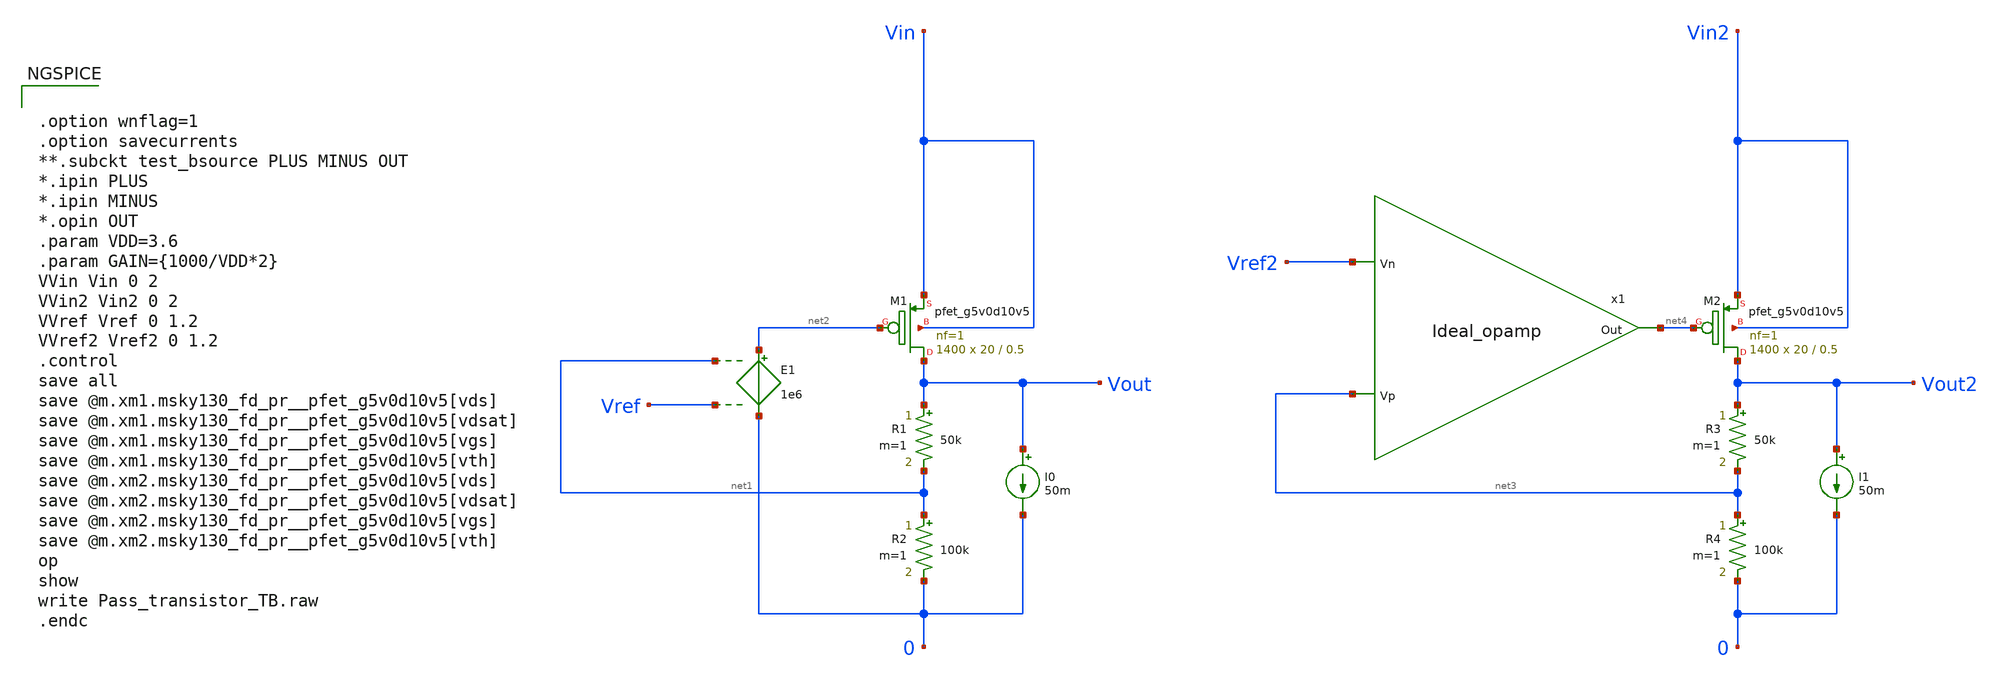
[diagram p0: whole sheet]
** sch_path: Analog_Blocks/LDO/Testbench/Pass_transistor_TB.sch
**.subckt Pass_transistor_TB
XM1 Vout net2 Vin Vin sky130_fd_pr__pfet_g5v0d10v5 L=0.5 W=20 nf=1 ad='int((nf+1)/2) * W/nf * 0.29' as='int((nf+2)/2) * W/nf * 0.29'
+ pd='2*int((nf+1)/2) * (W/nf + 0.29)' ps='2*int((nf+2)/2) * (W/nf + 0.29)' nrd='0.29 / W' nrs='0.29 / W'
+ sa=0 sb=0 sd=0 mult=1400 m=1400
R1 Vout net1 50k m=1
R2 net1 0 100k m=1
E1 net2 0 net1 Vref 1e6
I0 Vout 0 50m
XM2 Vout2 net4 Vin2 Vin2 sky130_fd_pr__pfet_g5v0d10v5 L=0.5 W=20 nf=1 ad='int((nf+1)/2) * W/nf * 0.29'
+ as='int((nf+2)/2) * W/nf * 0.29' pd='2*int((nf+1)/2) * (W/nf + 0.29)' ps='2*int((nf+2)/2) * (W/nf + 0.29)'
+ nrd='0.29 / W' nrs='0.29 / W' sa=0 sb=0 sd=0 mult=1400 m=1400
R3 Vout2 net3 50k m=1
R4 net3 0 100k m=1
I1 Vout2 0 50m
x1 net3 net4 Vref2 Ideal_opamp
**** begin user architecture code


.option wnflag=1
.option savecurrents
**.subckt test_bsource PLUS MINUS OUT
*.ipin PLUS
*.ipin MINUS
*.opin OUT
.param VDD=3.6
.param GAIN={1000/VDD*2}
VVin Vin 0 2
VVin2 Vin2 0 2
VVref Vref 0 1.2
VVref2 Vref2 0 1.2
.control
save all
save @m.xm1.msky130_fd_pr__pfet_g5v0d10v5[vds]
save @m.xm1.msky130_fd_pr__pfet_g5v0d10v5[vdsat]
save @m.xm1.msky130_fd_pr__pfet_g5v0d10v5[vgs]
save @m.xm1.msky130_fd_pr__pfet_g5v0d10v5[vth]
save @m.xm2.msky130_fd_pr__pfet_g5v0d10v5[vds]
save @m.xm2.msky130_fd_pr__pfet_g5v0d10v5[vdsat]
save @m.xm2.msky130_fd_pr__pfet_g5v0d10v5[vgs]
save @m.xm2.msky130_fd_pr__pfet_g5v0d10v5[vth]
op
show
write Pass_transistor_TB.raw
.endc




.param mc_mm_switch=0
.param mc_pr_switch=0
.include ~/mabrains/Analog_blocks/models/sky130A/libs.ref/sky130_fd_pr/spice/sky130_fd_pr__nfet_01v8__sf.corner.spice
.include ~/mabrains/Analog_blocks/models/sky130A/libs.ref/sky130_fd_pr/spice/sky130_fd_pr__nfet_01v8_lvt__sf.corner.spice
.include ~/mabrains/Analog_blocks/models/sky130A/libs.ref/sky130_fd_pr/spice/sky130_fd_pr__pfet_01v8__sf.corner.spice
.include ~/mabrains/Analog_blocks/models/sky130A/libs.ref/sky130_fd_pr/spice/sky130_fd_pr__nfet_03v3_nvt__sf.corner.spice
.include ~/mabrains/Analog_blocks/models/sky130A/libs.ref/sky130_fd_pr/spice/sky130_fd_pr__nfet_05v0_nvt__sf.corner.spice
.include ~/mabrains/Analog_blocks/models/sky130A/libs.ref/sky130_fd_pr/spice/sky130_fd_pr__esd_nfet_01v8__sf.corner.spice
.include ~/mabrains/Analog_blocks/models/sky130A/libs.ref/sky130_fd_pr/spice/sky130_fd_pr__pfet_01v8_lvt__sf.corner.spice
.include ~/mabrains/Analog_blocks/models/sky130A/libs.ref/sky130_fd_pr/spice/sky130_fd_pr__pfet_01v8_hvt__sf.corner.spice
.include ~/mabrains/Analog_blocks/models/sky130A/libs.ref/sky130_fd_pr/spice/sky130_fd_pr__esd_pfet_g5v0d10v5__sf.corner.spice
.include ~/mabrains/Analog_blocks/models/sky130A/libs.ref/sky130_fd_pr/spice/sky130_fd_pr__pfet_g5v0d10v5__sf.corner.spice
.include ~/mabrains/Analog_blocks/models/sky130A/libs.ref/sky130_fd_pr/spice/sky130_fd_pr__pfet_g5v0d16v0__sf.corner.spice
.include ~/mabrains/Analog_blocks/models/sky130A/libs.ref/sky130_fd_pr/spice/sky130_fd_pr__nfet_g5v0d10v5__sf.corner.spice
.include ~/mabrains/Analog_blocks/models/sky130A/libs.ref/sky130_fd_pr/spice/sky130_fd_pr__nfet_g5v0d16v0__sf_discrete.corner.spice
.include ~/mabrains/Analog_blocks/models/sky130A/libs.ref/sky130_fd_pr/spice/sky130_fd_pr__esd_nfet_g5v0d10v5__sf.corner.spice
.include ~/mabrains/Analog_blocks/models/sky130A/libs.ref/sky130_fd_pr/spice/sky130_fd_pr__pfet_20v0__sf_discrete.corner.spice
.include ~/mabrains/Analog_blocks/models/sky130A/libs.ref/sky130_fd_pr/spice/sky130_fd_pr__nfet_20v0__sf_discrete.corner.spice
.include ~/mabrains/Analog_blocks/models/sky130A/libs.tech/ngspice/corners/sf/nonfet.spice
* Mismatch parameters
.include ~/mabrains/Analog_blocks/models/sky130A/libs.ref/sky130_fd_pr/spice/sky130_fd_pr__nfet_01v8__mismatch.corner.spice
.include ~/mabrains/Analog_blocks/models/sky130A/libs.ref/sky130_fd_pr/spice/sky130_fd_pr__pfet_01v8__mismatch.corner.spice
.include ~/mabrains/Analog_blocks/models/sky130A/libs.ref/sky130_fd_pr/spice/sky130_fd_pr__nfet_01v8_lvt__mismatch.corner.spice
.include ~/mabrains/Analog_blocks/models/sky130A/libs.ref/sky130_fd_pr/spice/sky130_fd_pr__pfet_01v8_lvt__mismatch.corner.spice
.include ~/mabrains/Analog_blocks/models/sky130A/libs.ref/sky130_fd_pr/spice/sky130_fd_pr__pfet_01v8_hvt__mismatch.corner.spice
.include ~/mabrains/Analog_blocks/models/sky130A/libs.ref/sky130_fd_pr/spice/sky130_fd_pr__nfet_g5v0d10v5__mismatch.corner.spice
.include ~/mabrains/Analog_blocks/models/sky130A/libs.ref/sky130_fd_pr/spice/sky130_fd_pr__pfet_g5v0d10v5__mismatch.corner.spice
.include ~/mabrains/Analog_blocks/models/sky130A/libs.ref/sky130_fd_pr/spice/sky130_fd_pr__nfet_05v0_nvt__mismatch.corner.spice
.include ~/mabrains/Analog_blocks/models/sky130A/libs.ref/sky130_fd_pr/spice/sky130_fd_pr__nfet_03v3_nvt__mismatch.corner.spice
* Resistor/Capacitor
.include ~/mabrains/Analog_blocks/models/sky130A/libs.tech/ngspice/r+c/res_typical__cap_typical.spice
.include ~/mabrains/Analog_blocks/models/sky130A/libs.tech/ngspice/r+c/res_typical__cap_typical__lin.spice
* Special cells
.include ~/mabrains/Analog_blocks/models/sky130A/libs.tech/ngspice/corners/sf/specialized_cells.spice
* All models
.include ~/mabrains/Analog_blocks/models/sky130A/libs.tech/ngspice/all.spice
* Corner
.include ~/mabrains/Analog_blocks/models/sky130A/libs.tech/ngspice/corners/sf/rf.spice



**** end user architecture code
**.ends

* expanding   symbol:
*+  /home/eslam/mabrains/Analog_blocks/Analog_Blocks/OTA/Schematic/Ideal_opamp/Ideal_opamp.sym # of pins=3
** sym_path: Analog_blocks/Analog_Blocks/OTA/Schematic/Ideal_opamp/Ideal_opamp.sym
** sch_path: Analog_blocks/Analog_Blocks/OTA/Schematic/Ideal_opamp/Ideal_opamp.sch
.subckt Ideal_opamp Vp Out Vn
*.ipin Vp
*.ipin Vn
*.opin Out
V1 Vp PLUS_I 0
.save i(v1)
V2 Vn MINUS_I 0
.save i(v2)
B1 Out 0 V = 'VDD/2*(1+tanh(GAIN*(V(PLUS_I)-V(MINUS_I))))'
.ends

.end
